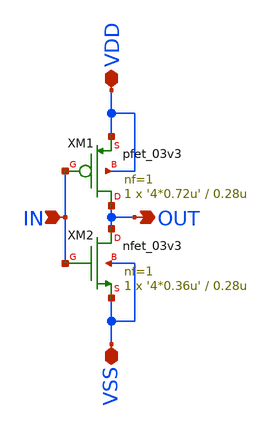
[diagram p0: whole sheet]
** sch_path: CAD7/four_inv.sch
**.subckt four_inv IN OUT VDD VSS
*.ipin IN
*.opin OUT
*.iopin VDD
*.iopin VSS
XM1 OUT IN VDD VDD pfet_03v3 L=0.28u W='4*0.72u' nf=1 ad='int((nf+1)/2) * W/nf * 0.18u' as='int((nf+2)/2) * W/nf * 0.18u'
+ pd='2*int((nf+1)/2) * (W/nf + 0.18u)' ps='2*int((nf+2)/2) * (W/nf + 0.18u)' nrd='0.18u / W' nrs='0.18u / W'
+ sa=0 sb=0 sd=0 m=1
XM2 OUT IN VSS VSS nfet_03v3 L=0.28u W='4*0.36u' nf=1 ad='int((nf+1)/2) * W/nf * 0.18u' as='int((nf+2)/2) * W/nf * 0.18u'
+ pd='2*int((nf+1)/2) * (W/nf + 0.18u)' ps='2*int((nf+2)/2) * (W/nf + 0.18u)' nrd='0.18u / W' nrs='0.18u / W'
+ sa=0 sb=0 sd=0 m=1
**.ends
.end
